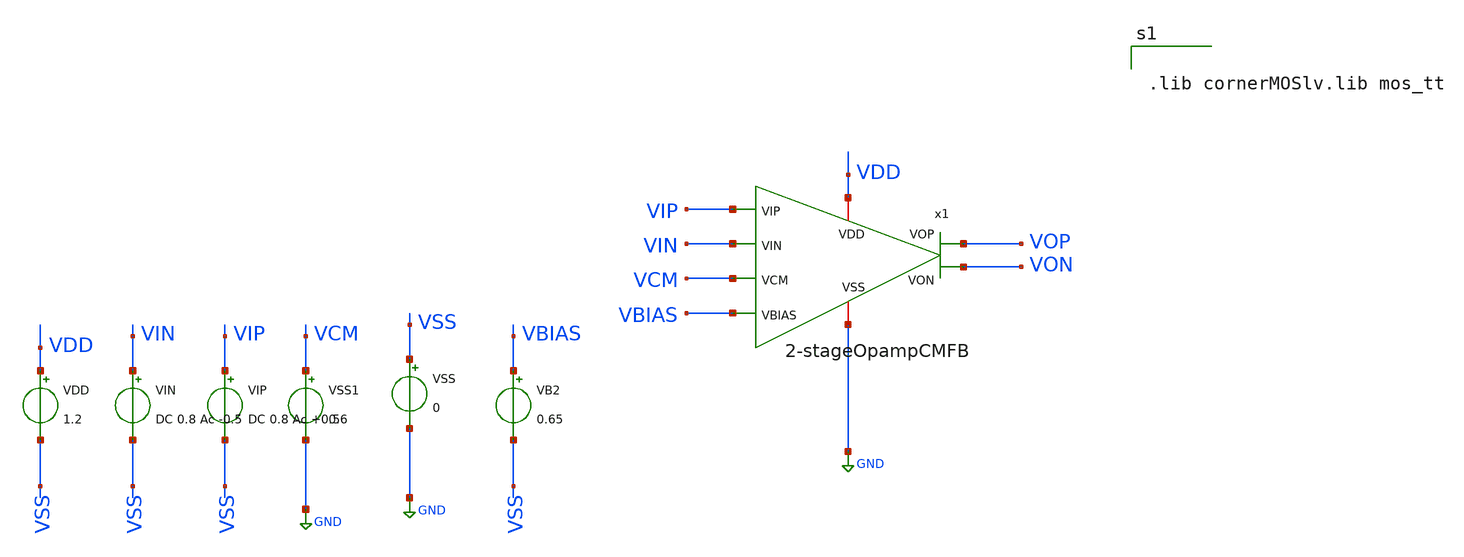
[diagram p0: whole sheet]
** sch_path: BTDay5-Ex/Test-2-stageOpampCMFB.sch
**.subckt Test-2-stageOpampCMFB
VDD VDD VSS 1.2
VIN VIN VSS DC 0.8 Ac -0.5
VIP VIP VSS DC 0.8 Ac +0.5
VSS VSS GND 0
VB2 VBIAS VSS 0.65
VSS1 VCM GND 0.6
x1 VCM VDD VBIAS VOP VON VIP VIN GND 2-stageOpampCMFB
**** begin user architecture code


.lib cornerMOSlv.lib mos_tt




.control
save all
op

* 1. IN DIEM LAM VIEC DC VA CONG SUAT
let power_mw = abs(i(vdd)[0]) * 1.2 * 1000
echo ================= KET QUA DC & CONG SUAT =================
print v(vip) v(vin) v(vbias) v(vcm) v(vop) v(von)
print power_mw

* 2. MO PHONG AC
ac dec 100 1 10G

* Tinh toan vi sai VOP va VON
let vid = v(vip) - v(vin)
let vod = v(vop) - v(von)
let av = vod / vid
let gain_db = db(av)
let phase_deg = cph(av) * 180 / pi
let open_loop_gain_times = mag(av[0])

if phase_deg[0] > 90
  let phase_deg = phase_deg - 360
end

meas ac f_ug when gain_db=0 fall=1
meas ac phase_at_ug find phase_deg when gain_db=0 fall=1
let phase_margin = 180 + phase_at_ug

echo ================= KET QUA SPEC EX3 =================
echo Open Loop Gain (lan):
print open_loop_gain_times
echo DC Gain (dB):
print gain_db[0]
echo Bandwidth GBW f_ug:
print f_ug
echo Phase Margin:
print phase_margin
echo Cong suat Power (mW):
print power_mw
echo ===================================================

let line_0db = 0 * frequency
let line_m180 = -180 + 0 * frequency

plot gain_db phase_deg line_0db line_m180 xlog ylimit -360 80 title 'Ex3: Fully-Diff OpAmp with CMFB'
.endc


**** end user architecture code
**.ends

* expanding   symbol:  /foss/designs/BTDay5-Ex/2-stageOpampCMFB.sym # of pins=8
** sym_path: BTDay5-Ex/2-stageOpampCMFB.sym
** sch_path: BTDay5-Ex/2-stageOpampCMFB.sch
.subckt 2-stageOpampCMFB VCM VDD VBIAS VOP VON VIP VIN VSS
*.iopin VDD
*.iopin VSS
*.ipin VBIAS
*.opin VON
*.ipin VIN
*.ipin VIP
*.opin VOP
*.ipin VCM
XM1 net3 VIN net1 VSS sg13_lv_nmos w=4u l=1u ng=1 m=2 mm_ok=1
XM2 net2 VIP net1 VSS sg13_lv_nmos w=4u l=1u ng=1 m=2 mm_ok=1
XM3 net1 VCMFBG VSS VSS sg13_lv_nmos w=4u l=1u ng=1 m=4 mm_ok=1
XM4 net3 VB1 VDD VDD sg13_lv_pmos w=8u l=1u ng=1 m=2 mm_ok=1
XM7 VB2 VB2 VSS VSS sg13_lv_nmos w=4u l=1u ng=1 m=1 mm_ok=1
XM8 VB2 VBIAS VDD VDD sg13_lv_pmos w=2u l=6u ng=1 m=1 mm_ok=1
XM10 net2 VB1 VDD VDD sg13_lv_pmos w=8u l=1u ng=1 m=2 mm_ok=1
XM5 VOP VB2 VSS VSS sg13_lv_nmos w=4u l=1u ng=1 m=1 mm_ok=1
XM11 VOP net2 VDD VDD sg13_lv_pmos w=4u l=1u ng=1 m=1 mm_ok=1
C2 VOP net4 1.8p m=1
R1 net4 net2 50k m=1
XM9 VON VB2 VSS VSS sg13_lv_nmos w=4u l=1u ng=1 m=1 mm_ok=1
C3 net5 VON 1.8p m=1
R2 net3 net5 50k m=1
XM12 VB1 VB1 VDD VDD sg13_lv_pmos w=8u l=1u ng=1 m=1 mm_ok=1
XM13 VB1 VB2 VSS VSS sg13_lv_nmos w=4u l=1u ng=1 m=1 mm_ok=1
XM6 VON net3 VDD VDD sg13_lv_pmos w=4u l=1u ng=1 m=1 mm_ok=1
XM14 net7 VB1 VDD VDD sg13_lv_pmos w=8u l=1u ng=1 m=2 mm_ok=1
XM15 net6 VB1 VDD VDD sg13_lv_pmos w=8u l=1u ng=1 m=2 mm_ok=1
XM16 VCMFBG VOP net6 VDD sg13_lv_pmos w=8u l=1u ng=1 m=1 mm_ok=1
XM17 VCMFBL VCM net6 VDD sg13_lv_pmos w=8u l=1u ng=1 m=1 mm_ok=1
XM18 VCMFBL VCM net7 VDD sg13_lv_pmos w=8u l=1u ng=1 m=1 mm_ok=1
XM19 VCMFBG VON net7 VDD sg13_lv_pmos w=8u l=1u ng=1 m=1 mm_ok=1
XM20 VCMFBL VCMFBL VSS VSS sg13_lv_nmos w=4u l=1u ng=1 m=4 mm_ok=1
XM21 VCMFBG VCMFBG VSS VSS sg13_lv_nmos w=4u l=1u ng=1 m=4 mm_ok=1
.ends

.GLOBAL GND
.end
